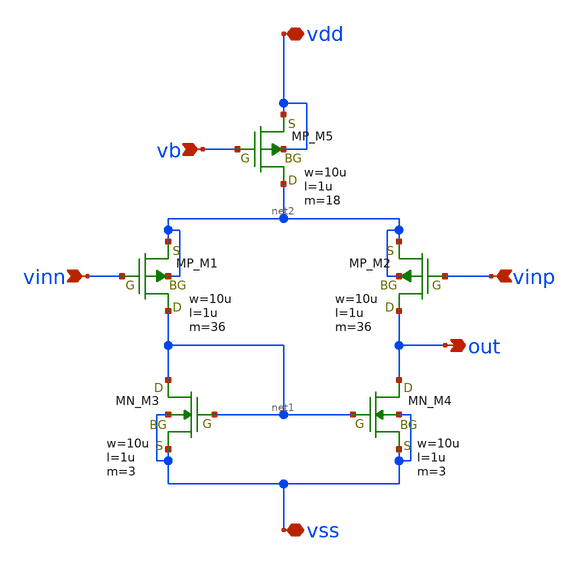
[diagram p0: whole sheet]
** sch_path: member_project/opamp/kubotakeshi/回路図/diff.sch
**.subckt diff vinn vinp vb out vdd vss
*.ipin vinn
*.ipin vinp
*.ipin vb
*.opin out
*.iopin vdd
*.iopin vss
XM5 net2 vb vdd vdd PMOS w=10u l=1u as=0 ad=0 ps=0 pd=0 nrd=0 nrs=0 m=18
XM1 net1 vinn net2 net2 PMOS w=10u l=1u as=0 ad=0 ps=0 pd=0 nrd=0 nrs=0 m=36
XM2 out vinp net2 net2 PMOS w=10u l=1u as=0 ad=0 ps=0 pd=0 nrd=0 nrs=0 m=36
XM3 net1 net1 vss vss NMOS w=10u l=1u as=0 ad=0 ps=0 pd=0 nrd=0 nrs=0 m=3
XM4 out net1 vss vss NMOS w=10u l=1u as=0 ad=0 ps=0 pd=0 nrd=0 nrs=0 m=3
**.ends
.end
